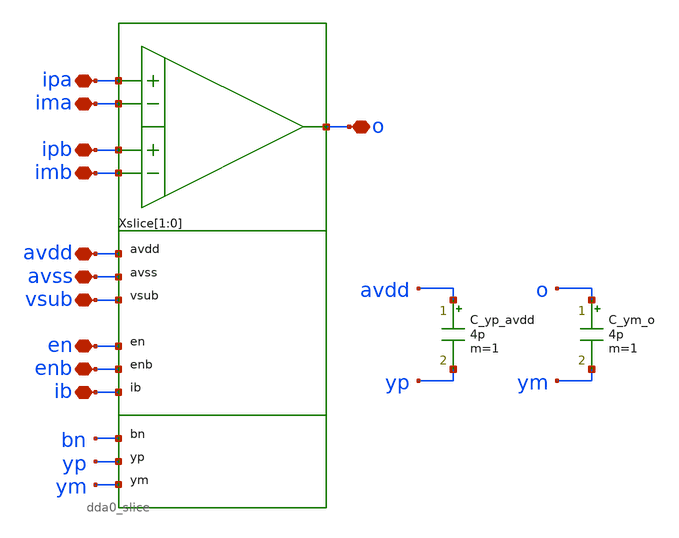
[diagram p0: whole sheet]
** sch_path: xschem/dda0.sch
**.subckt dda0 avdd avss ipa ima o ib vsub en enb ipb imb
*.iopin avdd
*.iopin avss
*.iopin ipa
*.iopin ima
*.iopin o
*.iopin ib
*.iopin vsub
*.iopin en
*.iopin enb
*.iopin ipb
*.iopin imb
Xslice[1] ipa ima ipb imb o avdd avss vsub en enb ib bn yp ym dda0_slice
Xslice[0] ipa ima ipb imb o avdd avss vsub en enb ib bn yp ym dda0_slice
C_yp_avdd avdd yp 4p m=1
C_ym_o o ym 4p m=1
**.ends
.end
